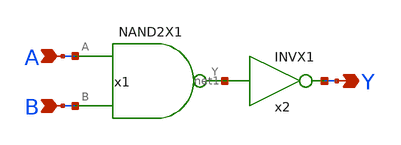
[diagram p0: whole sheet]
** sch_path: lib/xschem/AND2X1.sch
**.subckt AND2X1 A B Y
*.ipin A
*.ipin B
*.opin Y
x1 net1 A B NAND2X1
x2 Y net1 INVX1
**.ends

* expanding   symbol:  NAND2X1.sym # of pins=3
** sym_path: lib/xschem/NAND2X1.sym
** sch_path: lib/xschem/NAND2X1.sch
.subckt NAND2X1 Y A B
*.ipin A
*.opin Y
*.ipin B
XM1 Y A VDD VDD sky130_fd_pr__pfet_01v8 L=0.15 W=2 nf=1 ad='int((nf+1)/2) * W/nf * 0.29' as='int((nf+2)/2) * W/nf * 0.29'
+ pd='2*int((nf+1)/2) * (W/nf + 0.29)' ps='2*int((nf+2)/2) * (W/nf + 0.29)' nrd='0.29 / W' nrs='0.29 / W'
+ sa=0 sb=0 sd=0 mult=1 m=1
XM5 Y A net1 GND sky130_fd_pr__nfet_01v8 L=0.15 W=3 nf=1 ad='int((nf+1)/2) * W/nf * 0.29' as='int((nf+2)/2) * W/nf * 0.29'
+ pd='2*int((nf+1)/2) * (W/nf + 0.29)' ps='2*int((nf+2)/2) * (W/nf + 0.29)' nrd='0.29 / W' nrs='0.29 / W'
+ sa=0 sb=0 sd=0 mult=1 m=1
XM2 Y A VDD VDD sky130_fd_pr__pfet_01v8 L=0.15 W=2 nf=1 ad='int((nf+1)/2) * W/nf * 0.29' as='int((nf+2)/2) * W/nf * 0.29'
+ pd='2*int((nf+1)/2) * (W/nf + 0.29)' ps='2*int((nf+2)/2) * (W/nf + 0.29)' nrd='0.29 / W' nrs='0.29 / W'
+ sa=0 sb=0 sd=0 mult=1 m=1
XM3 Y B VDD VDD sky130_fd_pr__pfet_01v8 L=0.15 W=2 nf=1 ad='int((nf+1)/2) * W/nf * 0.29' as='int((nf+2)/2) * W/nf * 0.29'
+ pd='2*int((nf+1)/2) * (W/nf + 0.29)' ps='2*int((nf+2)/2) * (W/nf + 0.29)' nrd='0.29 / W' nrs='0.29 / W'
+ sa=0 sb=0 sd=0 mult=1 m=1
XM4 Y B VDD VDD sky130_fd_pr__pfet_01v8 L=0.15 W=2 nf=1 ad='int((nf+1)/2) * W/nf * 0.29' as='int((nf+2)/2) * W/nf * 0.29'
+ pd='2*int((nf+1)/2) * (W/nf + 0.29)' ps='2*int((nf+2)/2) * (W/nf + 0.29)' nrd='0.29 / W' nrs='0.29 / W'
+ sa=0 sb=0 sd=0 mult=1 m=1
XM6 net1 B GND GND sky130_fd_pr__nfet_01v8 L=0.15 W=3 nf=1 ad='int((nf+1)/2) * W/nf * 0.29' as='int((nf+2)/2) * W/nf * 0.29'
+ pd='2*int((nf+1)/2) * (W/nf + 0.29)' ps='2*int((nf+2)/2) * (W/nf + 0.29)' nrd='0.29 / W' nrs='0.29 / W'
+ sa=0 sb=0 sd=0 mult=1 m=1
.ends

.GLOBAL GND
.GLOBAL VDD
.end
